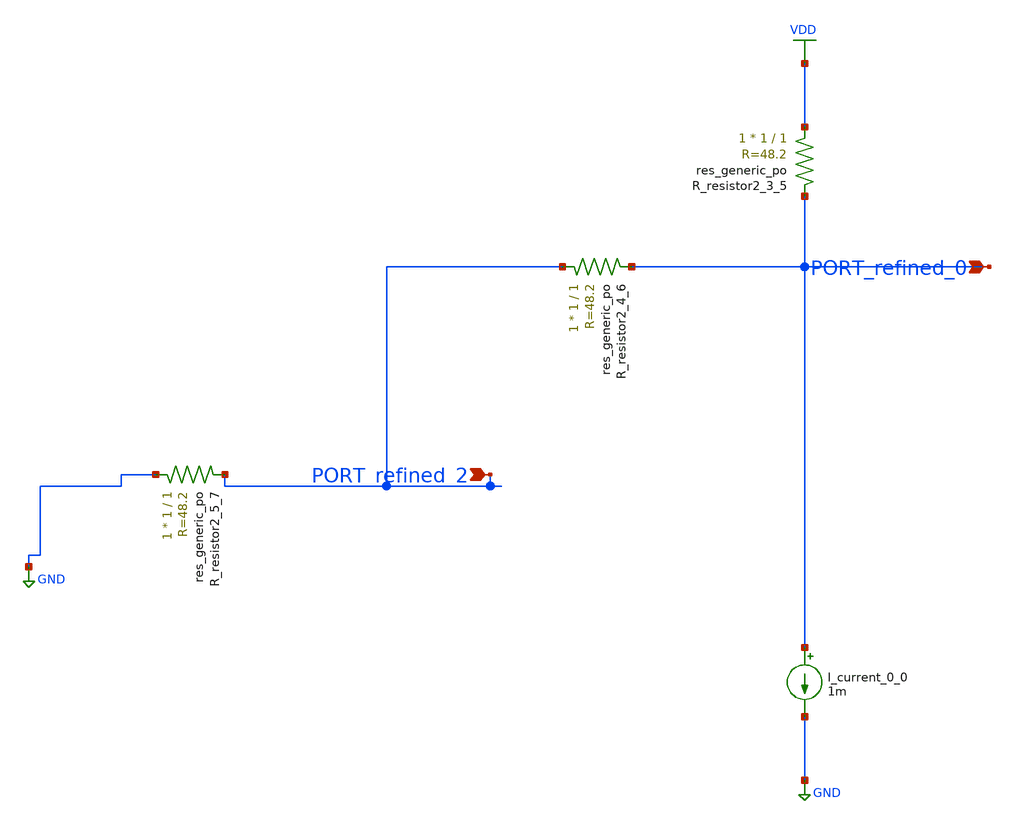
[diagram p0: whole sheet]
** sch_path: schematics/AMSNet/586.sch
**.subckt 586 PORT_refined_0 PORT_refined_2
*.ipin PORT_refined_0
*.ipin PORT_refined_2
I_current_0_0 PORT_refined_0 GND 1m
XR_resistor2_3_5 VDD PORT_refined_0 sky130_fd_pr__res_generic_po W=1 L=1 m=1
XR_resistor2_4_6 PORT_refined_2 PORT_refined_0 sky130_fd_pr__res_generic_po W=1 L=1 m=1
XR_resistor2_5_7 GND PORT_refined_2 sky130_fd_pr__res_generic_po W=1 L=1 m=1
**.ends
.GLOBAL GND
.GLOBAL VDD
.end
